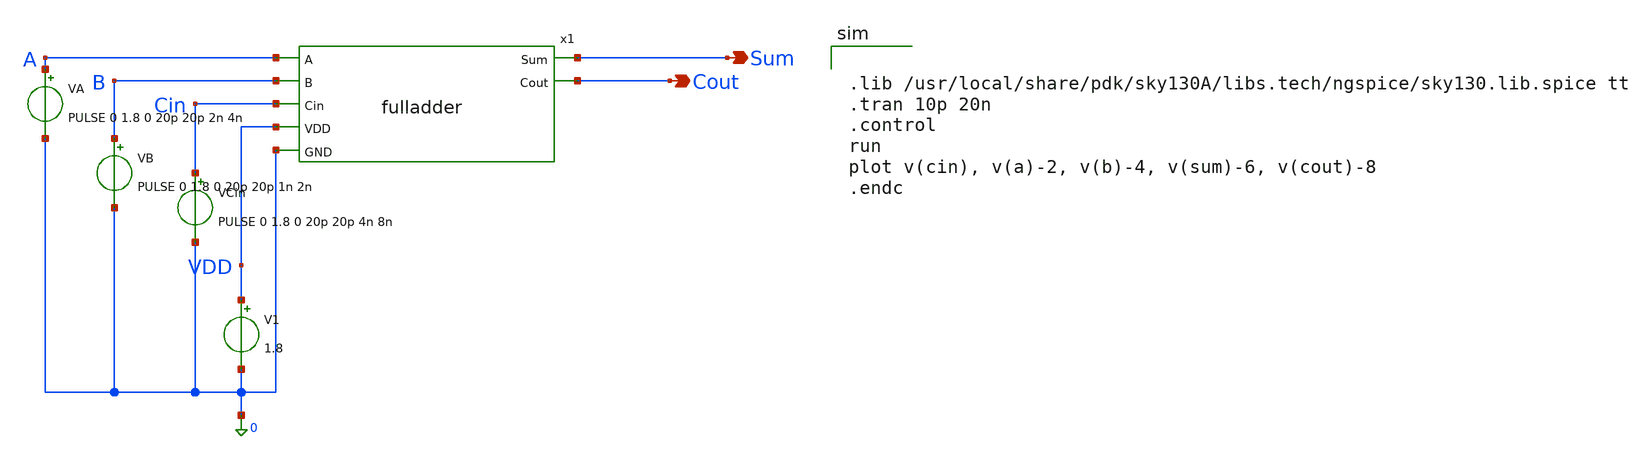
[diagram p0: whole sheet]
** sch_path: transmission_gate/testbench/fa_tb_tran.sch
**.subckt fa_tb_tran Sum Cout
*.opin Sum
*.opin Cout
V1 VDD 0 1.8
VA A 0 PULSE 0 1.8 0 20p 20p 2n 4n
VB B 0 PULSE 0 1.8 0 20p 20p 1n 2n
VCin Cin 0 PULSE 0 1.8 0 20p 20p 4n 8n
x1 A Sum B Cin VDD Cout 0 fulladder
**** begin user architecture code


.lib /usr/local/share/pdk/sky130A/libs.tech/ngspice/sky130.lib.spice tt
.tran 10p 20n
.control
run
plot v(cin), v(a)-2, v(b)-4, v(sum)-6, v(cout)-8
.endc


**** end user architecture code
**.ends

* expanding   symbol:
*+  /home/dat02/projects/cmos-full-adder-sky130/transmission_gate/schematic/fulladder.sym # of pins=7
** sym_path: transmission_gate/schematic/fulladder.sym
** sch_path: transmission_gate/schematic/fulladder.sch
.subckt fulladder A Sum B Cin VDD Cout GND
*.opin Cout
*.ipin A
*.ipin B
*.ipin Cin
*.opin Sum
*.ipin VDD
*.ipin GND
XM1 Cout net4 A VDD sky130_fd_pr__pfet_01v8 L=0.15 W=1.295 nf=1 ad='int((1 + 1)/2) * 1.295 / 1 * 0.29'
+ as='int((1 + 2)/2) * 1.295 / 1 * 0.29' pd='2*int((1 + 1)/2) * (1.295 / 1 + 0.29)' ps='2*int((1 + 2)/2) * (1.295 / 1 + 0.29)'
+ nrd='0.29 / 1.295 ' nrs='0.29 / 1.295 ' sa=0 sb=0 sd=0 mult=1 m=1
XM2 Cout net1 A GND sky130_fd_pr__nfet_01v8 L=0.15 W=0.42 nf=1 ad='int((1 + 1)/2) * 0.42 / 1 * 0.29'
+ as='int((1 + 2)/2) * 0.42 / 1 * 0.29' pd='2*int((1 + 1)/2) * (0.42 / 1 + 0.29)' ps='2*int((1 + 2)/2) * (0.42 / 1 + 0.29)'
+ nrd='0.29 / 0.42 ' nrs='0.29 / 0.42 ' sa=0 sb=0 sd=0 mult=1 m=1
XM3 Cout net1 Cin VDD sky130_fd_pr__pfet_01v8 L=0.15 W=1.295 nf=1 ad='int((1 + 1)/2) * 1.295 / 1 * 0.29'
+ as='int((1 + 2)/2) * 1.295 / 1 * 0.29' pd='2*int((1 + 1)/2) * (1.295 / 1 + 0.29)' ps='2*int((1 + 2)/2) * (1.295 / 1 + 0.29)'
+ nrd='0.29 / 1.295 ' nrs='0.29 / 1.295 ' sa=0 sb=0 sd=0 mult=1 m=1
XM4 Cout net4 Cin GND sky130_fd_pr__nfet_01v8 L=0.15 W=0.42 nf=1 ad='int((1 + 1)/2) * 0.42 / 1 * 0.29'
+ as='int((1 + 2)/2) * 0.42 / 1 * 0.29' pd='2*int((1 + 1)/2) * (0.42 / 1 + 0.29)' ps='2*int((1 + 2)/2) * (0.42 / 1 + 0.29)'
+ nrd='0.29 / 0.42 ' nrs='0.29 / 0.42 ' sa=0 sb=0 sd=0 mult=1 m=1
XM7 net2 A VDD VDD sky130_fd_pr__pfet_01v8 L=0.15 W=1.885 nf=1 ad='int((1 + 1)/2) * 1.885 / 1 * 0.29'
+ as='int((1 + 2)/2) * 1.885 / 1 * 0.29' pd='2*int((1 + 1)/2) * (1.885 / 1 + 0.29)' ps='2*int((1 + 2)/2) * (1.885 / 1 + 0.29)'
+ nrd='0.29 / 1.885 ' nrs='0.29 / 1.885 ' sa=0 sb=0 sd=0 mult=1 m=1
XM8 net2 A GND GND sky130_fd_pr__nfet_01v8 L=0.15 W=0.61 nf=1 ad='int((1 + 1)/2) * 0.61 / 1 * 0.29' as='int((1 + 2)/2) * 0.61 / 1 * 0.29'
+ pd='2*int((1 + 1)/2) * (0.61 / 1 + 0.29)' ps='2*int((1 + 2)/2) * (0.61 / 1 + 0.29)' nrd='0.29 / 0.61 '
+ nrs='0.29 / 0.61 ' sa=0 sb=0 sd=0 mult=1 m=1
XM9 net3 B VDD VDD sky130_fd_pr__pfet_01v8 L=0.15 W=1.885 nf=1 ad='int((1 + 1)/2) * 1.885 / 1 * 0.29'
+ as='int((1 + 2)/2) * 1.885 / 1 * 0.29' pd='2*int((1 + 1)/2) * (1.885 / 1 + 0.29)' ps='2*int((1 + 2)/2) * (1.885 / 1 + 0.29)'
+ nrd='0.29 / 1.885 ' nrs='0.29 / 1.885 ' sa=0 sb=0 sd=0 mult=1 m=1
XM10 net3 B GND GND sky130_fd_pr__nfet_01v8 L=0.15 W=0.61 nf=1 ad='int((1 + 1)/2) * 0.61 / 1 * 0.29'
+ as='int((1 + 2)/2) * 0.61 / 1 * 0.29' pd='2*int((1 + 1)/2) * (0.61 / 1 + 0.29)' ps='2*int((1 + 2)/2) * (0.61 / 1 + 0.29)'
+ nrd='0.29 / 0.61 ' nrs='0.29 / 0.61 ' sa=0 sb=0 sd=0 mult=1 m=1
XM11 net4 A B VDD sky130_fd_pr__pfet_01v8 L=0.15 W=1.885 nf=1 ad='int((1 + 1)/2) * 1.885 / 1 * 0.29'
+ as='int((1 + 2)/2) * 1.885 / 1 * 0.29' pd='2*int((1 + 1)/2) * (1.885 / 1 + 0.29)' ps='2*int((1 + 2)/2) * (1.885 / 1 + 0.29)'
+ nrd='0.29 / 1.885 ' nrs='0.29 / 1.885 ' sa=0 sb=0 sd=0 mult=1 m=1
XM12 net4 net2 B GND sky130_fd_pr__nfet_01v8 L=0.15 W=0.61 nf=1 ad='int((1 + 1)/2) * 0.61 / 1 * 0.29'
+ as='int((1 + 2)/2) * 0.61 / 1 * 0.29' pd='2*int((1 + 1)/2) * (0.61 / 1 + 0.29)' ps='2*int((1 + 2)/2) * (0.61 / 1 + 0.29)'
+ nrd='0.29 / 0.61 ' nrs='0.29 / 0.61 ' sa=0 sb=0 sd=0 mult=1 m=1
XM13 net4 net2 net3 VDD sky130_fd_pr__pfet_01v8 L=0.15 W=1.885 nf=1 ad='int((1 + 1)/2) * 1.885 / 1 * 0.29'
+ as='int((1 + 2)/2) * 1.885 / 1 * 0.29' pd='2*int((1 + 1)/2) * (1.885 / 1 + 0.29)' ps='2*int((1 + 2)/2) * (1.885 / 1 + 0.29)'
+ nrd='0.29 / 1.885 ' nrs='0.29 / 1.885 ' sa=0 sb=0 sd=0 mult=1 m=1
XM14 net4 A net3 GND sky130_fd_pr__nfet_01v8 L=0.15 W=0.61 nf=1 ad='int((1 + 1)/2) * 0.61 / 1 * 0.29'
+ as='int((1 + 2)/2) * 0.61 / 1 * 0.29' pd='2*int((1 + 1)/2) * (0.61 / 1 + 0.29)' ps='2*int((1 + 2)/2) * (0.61 / 1 + 0.29)'
+ nrd='0.29 / 0.61 ' nrs='0.29 / 0.61 ' sa=0 sb=0 sd=0 mult=1 m=1
XM15 net1 net4 VDD VDD sky130_fd_pr__pfet_01v8 L=0.15 W=2.59 nf=1 ad='int((1 + 1)/2) * 2.59 / 1 * 0.29'
+ as='int((1 + 2)/2) * 2.59 / 1 * 0.29' pd='2*int((1 + 1)/2) * (2.59 / 1 + 0.29)' ps='2*int((1 + 2)/2) * (2.59 / 1 + 0.29)'
+ nrd='0.29 / 2.59 ' nrs='0.29 / 2.59 ' sa=0 sb=0 sd=0 mult=1 m=1
XM16 net1 net4 GND GND sky130_fd_pr__nfet_01v8 L=0.15 W=0.84 nf=1 ad='int((1 + 1)/2) * 0.84 / 1 * 0.29'
+ as='int((1 + 2)/2) * 0.84 / 1 * 0.29' pd='2*int((1 + 1)/2) * (0.84 / 1 + 0.29)' ps='2*int((1 + 2)/2) * (0.84 / 1 + 0.29)'
+ nrd='0.29 / 0.84 ' nrs='0.29 / 0.84 ' sa=0 sb=0 sd=0 mult=1 m=1
XM17 net5 Cin VDD VDD sky130_fd_pr__pfet_01v8 L=0.15 W=1.295 nf=1 ad='int((1 + 1)/2) * 1.295 / 1 * 0.29'
+ as='int((1 + 2)/2) * 1.295 / 1 * 0.29' pd='2*int((1 + 1)/2) * (1.295 / 1 + 0.29)' ps='2*int((1 + 2)/2) * (1.295 / 1 + 0.29)'
+ nrd='0.29 / 1.295 ' nrs='0.29 / 1.295 ' sa=0 sb=0 sd=0 mult=1 m=1
XM18 net5 Cin GND GND sky130_fd_pr__nfet_01v8 L=0.15 W=0.42 nf=1 ad='int((1 + 1)/2) * 0.42 / 1 * 0.29'
+ as='int((1 + 2)/2) * 0.42 / 1 * 0.29' pd='2*int((1 + 1)/2) * (0.42 / 1 + 0.29)' ps='2*int((1 + 2)/2) * (0.42 / 1 + 0.29)'
+ nrd='0.29 / 0.42 ' nrs='0.29 / 0.42 ' sa=0 sb=0 sd=0 mult=1 m=1
XM19 Sum net4 Cin VDD sky130_fd_pr__pfet_01v8 L=0.15 W=1.295 nf=1 ad='int((1 + 1)/2) * 1.295 / 1 * 0.29'
+ as='int((1 + 2)/2) * 1.295 / 1 * 0.29' pd='2*int((1 + 1)/2) * (1.295 / 1 + 0.29)' ps='2*int((1 + 2)/2) * (1.295 / 1 + 0.29)'
+ nrd='0.29 / 1.295 ' nrs='0.29 / 1.295 ' sa=0 sb=0 sd=0 mult=1 m=1
XM20 Sum net1 Cin GND sky130_fd_pr__nfet_01v8 L=0.15 W=0.42 nf=1 ad='int((1 + 1)/2) * 0.42 / 1 * 0.29'
+ as='int((1 + 2)/2) * 0.42 / 1 * 0.29' pd='2*int((1 + 1)/2) * (0.42 / 1 + 0.29)' ps='2*int((1 + 2)/2) * (0.42 / 1 + 0.29)'
+ nrd='0.29 / 0.42 ' nrs='0.29 / 0.42 ' sa=0 sb=0 sd=0 mult=1 m=1
XM21 Sum net1 net5 VDD sky130_fd_pr__pfet_01v8 L=0.15 W=1.295 nf=1 ad='int((1 + 1)/2) * 1.295 / 1 * 0.29'
+ as='int((1 + 2)/2) * 1.295 / 1 * 0.29' pd='2*int((1 + 1)/2) * (1.295 / 1 + 0.29)' ps='2*int((1 + 2)/2) * (1.295 / 1 + 0.29)'
+ nrd='0.29 / 1.295 ' nrs='0.29 / 1.295 ' sa=0 sb=0 sd=0 mult=1 m=1
XM22 Sum net4 net5 GND sky130_fd_pr__nfet_01v8 L=0.15 W=0.42 nf=1 ad='int((1 + 1)/2) * 0.42 / 1 * 0.29'
+ as='int((1 + 2)/2) * 0.42 / 1 * 0.29' pd='2*int((1 + 1)/2) * (0.42 / 1 + 0.29)' ps='2*int((1 + 2)/2) * (0.42 / 1 + 0.29)'
+ nrd='0.29 / 0.42 ' nrs='0.29 / 0.42 ' sa=0 sb=0 sd=0 mult=1 m=1
.ends

.GLOBAL GND
.GLOBAL VDD
.end
